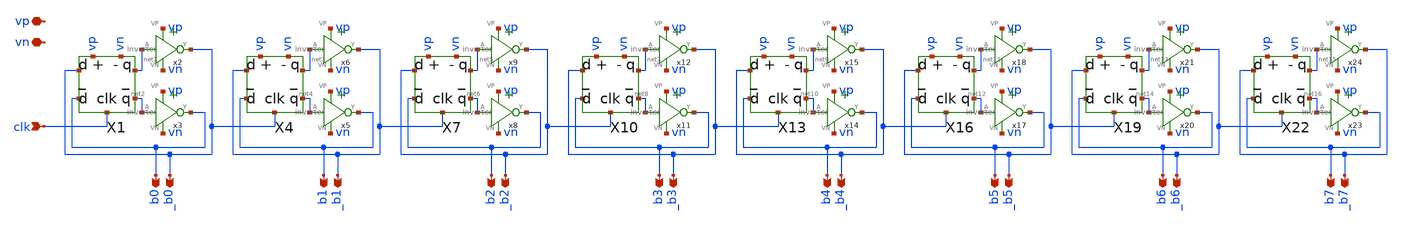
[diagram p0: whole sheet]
** sch_path: xschem/logic_gates/counter.sch
**.subckt counter vp vn clk b0 _b0 b1 _b1 b2 _b2 b3 _b3 b4 _b4 b5 _b5 b6 _b6 b7 _b7
*.iopin vp
*.iopin vn
*.ipin clk
*.opin b0
*.opin _b0
*.opin b1
*.opin _b1
*.opin b2
*.opin _b2
*.opin b3
*.opin _b3
*.opin b4
*.opin _b4
*.opin b5
*.opin _b5
*.opin b6
*.opin _b6
*.opin b7
*.opin _b7
X1 net2 net1 _b0 b0 clk vp vn dflipflop
x3 vp net2 b0 vn inverter
x2 vp net1 _b0 vn inverter
X4 net4 net3 _b1 b1 _b0 vp vn dflipflop
x5 vp net4 b1 vn inverter
x6 vp net3 _b1 vn inverter
X7 net6 net5 _b2 b2 _b1 vp vn dflipflop
x8 vp net6 b2 vn inverter
x9 vp net5 _b2 vn inverter
X10 net8 net7 _b3 b3 _b2 vp vn dflipflop
x11 vp net8 b3 vn inverter
x12 vp net7 _b3 vn inverter
X13 net10 net9 _b4 b4 _b3 vp vn dflipflop
x14 vp net10 b4 vn inverter
x15 vp net9 _b4 vn inverter
X16 net12 net11 _b5 b5 _b4 vp vn dflipflop
x17 vp net12 b5 vn inverter
x18 vp net11 _b5 vn inverter
X19 net14 net13 _b6 b6 _b5 vp vn dflipflop
x20 vp net14 b6 vn inverter
x21 vp net13 _b6 vn inverter
X22 net16 net15 _b7 b7 _b6 vp vn dflipflop
x23 vp net16 b7 vn inverter
x24 vp net15 _b7 vn inverter
**.ends

* expanding   symbol:  /home/madvlsi/dev/git/magic-dds/xschem/logic_gates/dflipflop.sym # of pins=7
** sym_path: xschem/logic_gates/dflipflop.sym
** sch_path: xschem/logic_gates/dflipflop.sch
.subckt dflipflop q_bar q d d_bar clk vp vn
*.opin q
*.opin q_bar
*.iopin vp
*.iopin vn
*.ipin d_bar
*.ipin d
*.ipin clk
XM8 vp net2 net3 vp sky130_fd_pr__pfet_01v8 L=0.15 W=1 nf=1 ad='int((nf+1)/2) * W/nf * 0.29' as='int((nf+2)/2) * W/nf * 0.29'
+ pd='2*int((nf+1)/2) * (W/nf + 0.29)' ps='2*int((nf+2)/2) * (W/nf + 0.29)' nrd='0.29 / W' nrs='0.29 / W'
+ sa=0 sb=0 sd=0 mult=1 m=1
XM9 vp net3 net2 vp sky130_fd_pr__pfet_01v8 L=0.15 W=1 nf=1 ad='int((nf+1)/2) * W/nf * 0.29' as='int((nf+2)/2) * W/nf * 0.29'
+ pd='2*int((nf+1)/2) * (W/nf + 0.29)' ps='2*int((nf+2)/2) * (W/nf + 0.29)' nrd='0.29 / W' nrs='0.29 / W'
+ sa=0 sb=0 sd=0 mult=1 m=1
XM5 net1 clk vn vn sky130_fd_pr__nfet_01v8 L=0.15 W=1 nf=1 ad='int((nf+1)/2) * W/nf * 0.29' as='int((nf+2)/2) * W/nf * 0.29'
+ pd='2*int((nf+1)/2) * (W/nf + 0.29)' ps='2*int((nf+2)/2) * (W/nf + 0.29)' nrd='0.29 / W' nrs='0.29 / W'
+ sa=0 sb=0 sd=0 mult=1 m=1
XM6 net3 net2 net1 vn sky130_fd_pr__nfet_01v8 L=0.15 W=1 nf=1 ad='int((nf+1)/2) * W/nf * 0.29' as='int((nf+2)/2) * W/nf * 0.29'
+ pd='2*int((nf+1)/2) * (W/nf + 0.29)' ps='2*int((nf+2)/2) * (W/nf + 0.29)' nrd='0.29 / W' nrs='0.29 / W'
+ sa=0 sb=0 sd=0 mult=1 m=1
XM7 net2 net3 net1 vn sky130_fd_pr__nfet_01v8 L=0.15 W=1 nf=1 ad='int((nf+1)/2) * W/nf * 0.29' as='int((nf+2)/2) * W/nf * 0.29'
+ pd='2*int((nf+1)/2) * (W/nf + 0.29)' ps='2*int((nf+2)/2) * (W/nf + 0.29)' nrd='0.29 / W' nrs='0.29 / W'
+ sa=0 sb=0 sd=0 mult=1 m=1
XM13 vn q q_bar vn sky130_fd_pr__nfet_01v8 L=0.15 W=1 nf=1 ad='int((nf+1)/2) * W/nf * 0.29' as='int((nf+2)/2) * W/nf * 0.29'
+ pd='2*int((nf+1)/2) * (W/nf + 0.29)' ps='2*int((nf+2)/2) * (W/nf + 0.29)' nrd='0.29 / W' nrs='0.29 / W'
+ sa=0 sb=0 sd=0 mult=1 m=1
XM3 q clk net2 vn sky130_fd_pr__nfet_01v8 L=0.30 W=1 nf=1 ad='int((nf+1)/2) * W/nf * 0.29' as='int((nf+2)/2) * W/nf * 0.29'
+ pd='2*int((nf+1)/2) * (W/nf + 0.29)' ps='2*int((nf+2)/2) * (W/nf + 0.29)' nrd='0.29 / W' nrs='0.29 / W'
+ sa=0 sb=0 sd=0 mult=1 m=1
XM4 q_bar clk net3 vn sky130_fd_pr__nfet_01v8 L=0.30 W=1 nf=1 ad='int((nf+1)/2) * W/nf * 0.29' as='int((nf+2)/2) * W/nf * 0.29'
+ pd='2*int((nf+1)/2) * (W/nf + 0.29)' ps='2*int((nf+2)/2) * (W/nf + 0.29)' nrd='0.29 / W' nrs='0.29 / W'
+ sa=0 sb=0 sd=0 mult=1 m=1
XM14 vn q_bar q vn sky130_fd_pr__nfet_01v8 L=0.15 W=1 nf=1 ad='int((nf+1)/2) * W/nf * 0.29' as='int((nf+2)/2) * W/nf * 0.29'
+ pd='2*int((nf+1)/2) * (W/nf + 0.29)' ps='2*int((nf+2)/2) * (W/nf + 0.29)' nrd='0.29 / W' nrs='0.29 / W'
+ sa=0 sb=0 sd=0 mult=1 m=1
XM10 net4 clk vp vp sky130_fd_pr__pfet_01v8 L=0.15 W=1 nf=1 ad='int((nf+1)/2) * W/nf * 0.29' as='int((nf+2)/2) * W/nf * 0.29'
+ pd='2*int((nf+1)/2) * (W/nf + 0.29)' ps='2*int((nf+2)/2) * (W/nf + 0.29)' nrd='0.29 / W' nrs='0.29 / W'
+ sa=0 sb=0 sd=0 mult=1 m=1
XM11 q_bar q net4 vp sky130_fd_pr__pfet_01v8 L=0.15 W=1 nf=1 ad='int((nf+1)/2) * W/nf * 0.29' as='int((nf+2)/2) * W/nf * 0.29'
+ pd='2*int((nf+1)/2) * (W/nf + 0.29)' ps='2*int((nf+2)/2) * (W/nf + 0.29)' nrd='0.29 / W' nrs='0.29 / W'
+ sa=0 sb=0 sd=0 mult=1 m=1
XM12 q q_bar net4 vp sky130_fd_pr__pfet_01v8 L=0.15 W=1 nf=1 ad='int((nf+1)/2) * W/nf * 0.29' as='int((nf+2)/2) * W/nf * 0.29'
+ pd='2*int((nf+1)/2) * (W/nf + 0.29)' ps='2*int((nf+2)/2) * (W/nf + 0.29)' nrd='0.29 / W' nrs='0.29 / W'
+ sa=0 sb=0 sd=0 mult=1 m=1
XM15 net1 clk vn vn sky130_fd_pr__nfet_01v8 L=0.15 W=1 nf=1 ad='int((nf+1)/2) * W/nf * 0.29' as='int((nf+2)/2) * W/nf * 0.29'
+ pd='2*int((nf+1)/2) * (W/nf + 0.29)' ps='2*int((nf+2)/2) * (W/nf + 0.29)' nrd='0.29 / W' nrs='0.29 / W'
+ sa=0 sb=0 sd=0 mult=1 m=1
XM16 net4 clk vp vp sky130_fd_pr__pfet_01v8 L=0.15 W=1 nf=1 ad='int((nf+1)/2) * W/nf * 0.29' as='int((nf+2)/2) * W/nf * 0.29'
+ pd='2*int((nf+1)/2) * (W/nf + 0.29)' ps='2*int((nf+2)/2) * (W/nf + 0.29)' nrd='0.29 / W' nrs='0.29 / W'
+ sa=0 sb=0 sd=0 mult=1 m=1
XM1 net2 clk d vp sky130_fd_pr__pfet_01v8 L=0.30 W=1 nf=1 ad='int((nf+1)/2) * W/nf * 0.29' as='int((nf+2)/2) * W/nf * 0.29'
+ pd='2*int((nf+1)/2) * (W/nf + 0.29)' ps='2*int((nf+2)/2) * (W/nf + 0.29)' nrd='0.29 / W' nrs='0.29 / W'
+ sa=0 sb=0 sd=0 mult=1 m=1
XM2 net3 clk d_bar vp sky130_fd_pr__pfet_01v8 L=0.30 W=1 nf=1 ad='int((nf+1)/2) * W/nf * 0.29' as='int((nf+2)/2) * W/nf * 0.29'
+ pd='2*int((nf+1)/2) * (W/nf + 0.29)' ps='2*int((nf+2)/2) * (W/nf + 0.29)' nrd='0.29 / W' nrs='0.29 / W'
+ sa=0 sb=0 sd=0 mult=1 m=1
.ends


* expanding   symbol:  /home/madvlsi/dev/git/magic-dds/xschem/other_project_files/inverter.sym # of
*+ pins=4
** sym_path: xschem/other_project_files/inverter.sym
** sch_path: xschem/other_project_files/inverter.sch
.subckt inverter VP A Y VN
*.iopin VP
*.iopin VN
*.ipin A
*.opin Y
XM1 Y A VN VN sky130_fd_pr__nfet_01v8 L=0.15 W=1 nf=1 ad='int((nf+1)/2) * W/nf * 0.29' as='int((nf+2)/2) * W/nf * 0.29'
+ pd='2*int((nf+1)/2) * (W/nf + 0.29)' ps='2*int((nf+2)/2) * (W/nf + 0.29)' nrd='0.29 / W' nrs='0.29 / W'
+ sa=0 sb=0 sd=0 mult=1 m=1
XM2 Y A VP VP sky130_fd_pr__pfet_01v8 L=0.15 W=4 nf=1 ad='int((nf+1)/2) * W/nf * 0.29' as='int((nf+2)/2) * W/nf * 0.29'
+ pd='2*int((nf+1)/2) * (W/nf + 0.29)' ps='2*int((nf+2)/2) * (W/nf + 0.29)' nrd='0.29 / W' nrs='0.29 / W'
+ sa=0 sb=0 sd=0 mult=1 m=1
.ends

.end
